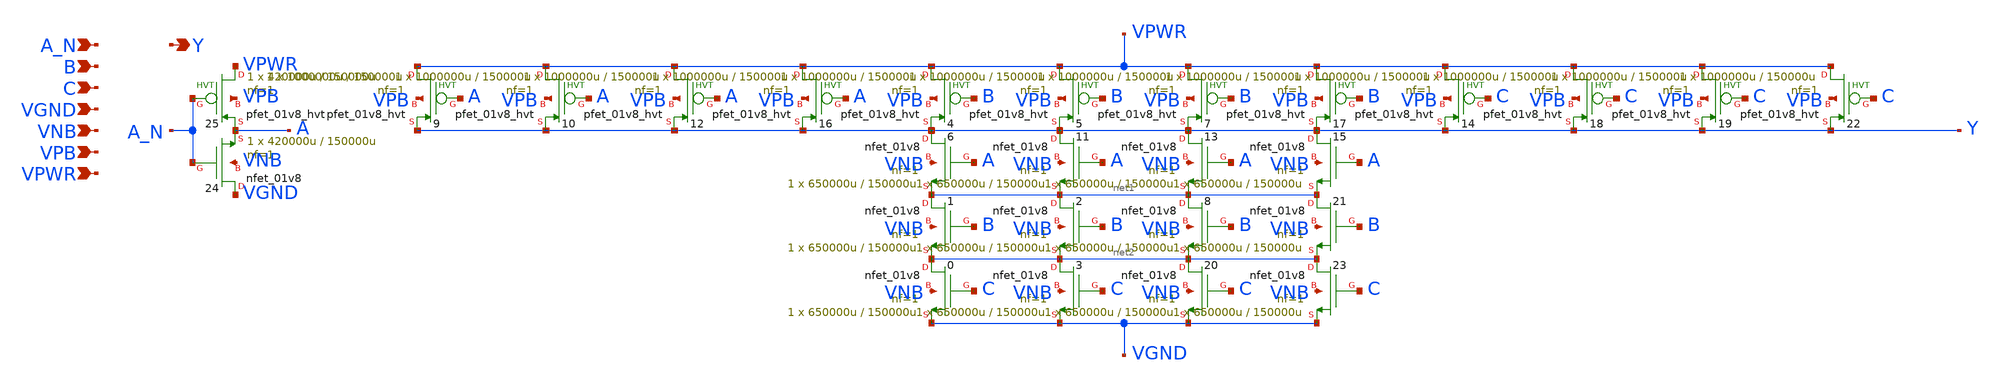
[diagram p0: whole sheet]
** sch_path: schematics/nand3b/sky130_fd_sc_hd__nand3b_4.sch
**.subckt sky130_fd_sc_hd__nand3b_4 A_N B C VGND VNB VPB VPWR Y
*.ipin A_N
*.ipin B
*.ipin C
*.ipin VGND
*.ipin VNB
*.ipin VPB
*.ipin VPWR
*.opin Y
X10 VPWR A Y VPB sky130_fd_pr__pfet_01v8_hvt L=150000u W=1000000u nf=1 ad='int((1 + 1)/2) * 1000000u / 1 * 0.29'
+ as='int((1 + 2)/2) * 1000000u / 1 * 0.29' pd='2*int((1 + 1)/2) * (1000000u / 1 + 0.29)' ps='2*int((1 + 2)/2) * (1000000u / 1 + 0.29)'
+ nrd='0.29 / 1000000u ' nrs='0.29 / 1000000u ' sa=0 sb=0 sd=0 mult=1 m=1
X9 VPWR A Y VPB sky130_fd_pr__pfet_01v8_hvt L=150000u W=1000000u nf=1 ad='int((1 + 1)/2) * 1000000u / 1 * 0.29'
+ as='int((1 + 2)/2) * 1000000u / 1 * 0.29' pd='2*int((1 + 1)/2) * (1000000u / 1 + 0.29)' ps='2*int((1 + 2)/2) * (1000000u / 1 + 0.29)'
+ nrd='0.29 / 1000000u ' nrs='0.29 / 1000000u ' sa=0 sb=0 sd=0 mult=1 m=1
X6 Y A net1 VNB sky130_fd_pr__nfet_01v8 L=150000u W=650000u nf=1 ad='int((1 + 1)/2) * 650000u / 1 * 0.29'
+ as='int((1 + 2)/2) * 650000u / 1 * 0.29' pd='2*int((1 + 1)/2) * (650000u / 1 + 0.29)' ps='2*int((1 + 2)/2) * (650000u / 1 + 0.29)'
+ nrd='0.29 / 650000u ' nrs='0.29 / 650000u ' sa=0 sb=0 sd=0 mult=1 m=1
X1 net1 B net2 VNB sky130_fd_pr__nfet_01v8 L=150000u W=650000u nf=1 ad='int((1 + 1)/2) * 650000u / 1 * 0.29'
+ as='int((1 + 2)/2) * 650000u / 1 * 0.29' pd='2*int((1 + 1)/2) * (650000u / 1 + 0.29)' ps='2*int((1 + 2)/2) * (650000u / 1 + 0.29)'
+ nrd='0.29 / 650000u ' nrs='0.29 / 650000u ' sa=0 sb=0 sd=0 mult=1 m=1
X12 VPWR A Y VPB sky130_fd_pr__pfet_01v8_hvt L=150000u W=1000000u nf=1 ad='int((1 + 1)/2) * 1000000u / 1 * 0.29'
+ as='int((1 + 2)/2) * 1000000u / 1 * 0.29' pd='2*int((1 + 1)/2) * (1000000u / 1 + 0.29)' ps='2*int((1 + 2)/2) * (1000000u / 1 + 0.29)'
+ nrd='0.29 / 1000000u ' nrs='0.29 / 1000000u ' sa=0 sb=0 sd=0 mult=1 m=1
X0 net2 C VGND VNB sky130_fd_pr__nfet_01v8 L=150000u W=650000u nf=1 ad='int((1 + 1)/2) * 650000u / 1 * 0.29'
+ as='int((1 + 2)/2) * 650000u / 1 * 0.29' pd='2*int((1 + 1)/2) * (650000u / 1 + 0.29)' ps='2*int((1 + 2)/2) * (650000u / 1 + 0.29)'
+ nrd='0.29 / 650000u ' nrs='0.29 / 650000u ' sa=0 sb=0 sd=0 mult=1 m=1
X4 VPWR B Y VPB sky130_fd_pr__pfet_01v8_hvt L=150000u W=1000000u nf=1 ad='int((1 + 1)/2) * 1000000u / 1 * 0.29'
+ as='int((1 + 2)/2) * 1000000u / 1 * 0.29' pd='2*int((1 + 1)/2) * (1000000u / 1 + 0.29)' ps='2*int((1 + 2)/2) * (1000000u / 1 + 0.29)'
+ nrd='0.29 / 1000000u ' nrs='0.29 / 1000000u ' sa=0 sb=0 sd=0 mult=1 m=1
X16 VPWR A Y VPB sky130_fd_pr__pfet_01v8_hvt L=150000u W=1000000u nf=1 ad='int((1 + 1)/2) * 1000000u / 1 * 0.29'
+ as='int((1 + 2)/2) * 1000000u / 1 * 0.29' pd='2*int((1 + 1)/2) * (1000000u / 1 + 0.29)' ps='2*int((1 + 2)/2) * (1000000u / 1 + 0.29)'
+ nrd='0.29 / 1000000u ' nrs='0.29 / 1000000u ' sa=0 sb=0 sd=0 mult=1 m=1
X5 VPWR B Y VPB sky130_fd_pr__pfet_01v8_hvt L=150000u W=1000000u nf=1 ad='int((1 + 1)/2) * 1000000u / 1 * 0.29'
+ as='int((1 + 2)/2) * 1000000u / 1 * 0.29' pd='2*int((1 + 1)/2) * (1000000u / 1 + 0.29)' ps='2*int((1 + 2)/2) * (1000000u / 1 + 0.29)'
+ nrd='0.29 / 1000000u ' nrs='0.29 / 1000000u ' sa=0 sb=0 sd=0 mult=1 m=1
X11 Y A net1 VNB sky130_fd_pr__nfet_01v8 L=150000u W=650000u nf=1 ad='int((1 + 1)/2) * 650000u / 1 * 0.29'
+ as='int((1 + 2)/2) * 650000u / 1 * 0.29' pd='2*int((1 + 1)/2) * (650000u / 1 + 0.29)' ps='2*int((1 + 2)/2) * (650000u / 1 + 0.29)'
+ nrd='0.29 / 650000u ' nrs='0.29 / 650000u ' sa=0 sb=0 sd=0 mult=1 m=1
X2 net1 B net2 VNB sky130_fd_pr__nfet_01v8 L=150000u W=650000u nf=1 ad='int((1 + 1)/2) * 650000u / 1 * 0.29'
+ as='int((1 + 2)/2) * 650000u / 1 * 0.29' pd='2*int((1 + 1)/2) * (650000u / 1 + 0.29)' ps='2*int((1 + 2)/2) * (650000u / 1 + 0.29)'
+ nrd='0.29 / 650000u ' nrs='0.29 / 650000u ' sa=0 sb=0 sd=0 mult=1 m=1
X3 net2 C VGND VNB sky130_fd_pr__nfet_01v8 L=150000u W=650000u nf=1 ad='int((1 + 1)/2) * 650000u / 1 * 0.29'
+ as='int((1 + 2)/2) * 650000u / 1 * 0.29' pd='2*int((1 + 1)/2) * (650000u / 1 + 0.29)' ps='2*int((1 + 2)/2) * (650000u / 1 + 0.29)'
+ nrd='0.29 / 650000u ' nrs='0.29 / 650000u ' sa=0 sb=0 sd=0 mult=1 m=1
X17 VPWR B Y VPB sky130_fd_pr__pfet_01v8_hvt L=150000u W=1000000u nf=1 ad='int((1 + 1)/2) * 1000000u / 1 * 0.29'
+ as='int((1 + 2)/2) * 1000000u / 1 * 0.29' pd='2*int((1 + 1)/2) * (1000000u / 1 + 0.29)' ps='2*int((1 + 2)/2) * (1000000u / 1 + 0.29)'
+ nrd='0.29 / 1000000u ' nrs='0.29 / 1000000u ' sa=0 sb=0 sd=0 mult=1 m=1
X7 VPWR B Y VPB sky130_fd_pr__pfet_01v8_hvt L=150000u W=1000000u nf=1 ad='int((1 + 1)/2) * 1000000u / 1 * 0.29'
+ as='int((1 + 2)/2) * 1000000u / 1 * 0.29' pd='2*int((1 + 1)/2) * (1000000u / 1 + 0.29)' ps='2*int((1 + 2)/2) * (1000000u / 1 + 0.29)'
+ nrd='0.29 / 1000000u ' nrs='0.29 / 1000000u ' sa=0 sb=0 sd=0 mult=1 m=1
X14 VPWR C Y VPB sky130_fd_pr__pfet_01v8_hvt L=150000u W=1000000u nf=1 ad='int((1 + 1)/2) * 1000000u / 1 * 0.29'
+ as='int((1 + 2)/2) * 1000000u / 1 * 0.29' pd='2*int((1 + 1)/2) * (1000000u / 1 + 0.29)' ps='2*int((1 + 2)/2) * (1000000u / 1 + 0.29)'
+ nrd='0.29 / 1000000u ' nrs='0.29 / 1000000u ' sa=0 sb=0 sd=0 mult=1 m=1
X19 VPWR C Y VPB sky130_fd_pr__pfet_01v8_hvt L=150000u W=1000000u nf=1 ad='int((1 + 1)/2) * 1000000u / 1 * 0.29'
+ as='int((1 + 2)/2) * 1000000u / 1 * 0.29' pd='2*int((1 + 1)/2) * (1000000u / 1 + 0.29)' ps='2*int((1 + 2)/2) * (1000000u / 1 + 0.29)'
+ nrd='0.29 / 1000000u ' nrs='0.29 / 1000000u ' sa=0 sb=0 sd=0 mult=1 m=1
X18 VPWR C Y VPB sky130_fd_pr__pfet_01v8_hvt L=150000u W=1000000u nf=1 ad='int((1 + 1)/2) * 1000000u / 1 * 0.29'
+ as='int((1 + 2)/2) * 1000000u / 1 * 0.29' pd='2*int((1 + 1)/2) * (1000000u / 1 + 0.29)' ps='2*int((1 + 2)/2) * (1000000u / 1 + 0.29)'
+ nrd='0.29 / 1000000u ' nrs='0.29 / 1000000u ' sa=0 sb=0 sd=0 mult=1 m=1
X22 VPWR C Y VPB sky130_fd_pr__pfet_01v8_hvt L=150000u W=1000000u nf=1 ad='int((1 + 1)/2) * 1000000u / 1 * 0.29'
+ as='int((1 + 2)/2) * 1000000u / 1 * 0.29' pd='2*int((1 + 1)/2) * (1000000u / 1 + 0.29)' ps='2*int((1 + 2)/2) * (1000000u / 1 + 0.29)'
+ nrd='0.29 / 1000000u ' nrs='0.29 / 1000000u ' sa=0 sb=0 sd=0 mult=1 m=1
X13 Y A net1 VNB sky130_fd_pr__nfet_01v8 L=150000u W=650000u nf=1 ad='int((1 + 1)/2) * 650000u / 1 * 0.29'
+ as='int((1 + 2)/2) * 650000u / 1 * 0.29' pd='2*int((1 + 1)/2) * (650000u / 1 + 0.29)' ps='2*int((1 + 2)/2) * (650000u / 1 + 0.29)'
+ nrd='0.29 / 650000u ' nrs='0.29 / 650000u ' sa=0 sb=0 sd=0 mult=1 m=1
X8 net1 B net2 VNB sky130_fd_pr__nfet_01v8 L=150000u W=650000u nf=1 ad='int((1 + 1)/2) * 650000u / 1 * 0.29'
+ as='int((1 + 2)/2) * 650000u / 1 * 0.29' pd='2*int((1 + 1)/2) * (650000u / 1 + 0.29)' ps='2*int((1 + 2)/2) * (650000u / 1 + 0.29)'
+ nrd='0.29 / 650000u ' nrs='0.29 / 650000u ' sa=0 sb=0 sd=0 mult=1 m=1
X20 net2 C VGND VNB sky130_fd_pr__nfet_01v8 L=150000u W=650000u nf=1 ad='int((1 + 1)/2) * 650000u / 1 * 0.29'
+ as='int((1 + 2)/2) * 650000u / 1 * 0.29' pd='2*int((1 + 1)/2) * (650000u / 1 + 0.29)' ps='2*int((1 + 2)/2) * (650000u / 1 + 0.29)'
+ nrd='0.29 / 650000u ' nrs='0.29 / 650000u ' sa=0 sb=0 sd=0 mult=1 m=1
X15 Y A net1 VNB sky130_fd_pr__nfet_01v8 L=150000u W=650000u nf=1 ad='int((1 + 1)/2) * 650000u / 1 * 0.29'
+ as='int((1 + 2)/2) * 650000u / 1 * 0.29' pd='2*int((1 + 1)/2) * (650000u / 1 + 0.29)' ps='2*int((1 + 2)/2) * (650000u / 1 + 0.29)'
+ nrd='0.29 / 650000u ' nrs='0.29 / 650000u ' sa=0 sb=0 sd=0 mult=1 m=1
X21 net1 B net2 VNB sky130_fd_pr__nfet_01v8 L=150000u W=650000u nf=1 ad='int((1 + 1)/2) * 650000u / 1 * 0.29'
+ as='int((1 + 2)/2) * 650000u / 1 * 0.29' pd='2*int((1 + 1)/2) * (650000u / 1 + 0.29)' ps='2*int((1 + 2)/2) * (650000u / 1 + 0.29)'
+ nrd='0.29 / 650000u ' nrs='0.29 / 650000u ' sa=0 sb=0 sd=0 mult=1 m=1
X23 net2 C VGND VNB sky130_fd_pr__nfet_01v8 L=150000u W=650000u nf=1 ad='int((1 + 1)/2) * 650000u / 1 * 0.29'
+ as='int((1 + 2)/2) * 650000u / 1 * 0.29' pd='2*int((1 + 1)/2) * (650000u / 1 + 0.29)' ps='2*int((1 + 2)/2) * (650000u / 1 + 0.29)'
+ nrd='0.29 / 650000u ' nrs='0.29 / 650000u ' sa=0 sb=0 sd=0 mult=1 m=1
X24 VGND A_N A VNB sky130_fd_pr__nfet_01v8 L=150000u W=420000u nf=1 ad='int((1 + 1)/2) * 420000u / 1 * 0.29'
+ as='int((1 + 2)/2) * 420000u / 1 * 0.29' pd='2*int((1 + 1)/2) * (420000u / 1 + 0.29)' ps='2*int((1 + 2)/2) * (420000u / 1 + 0.29)'
+ nrd='0.29 / 420000u ' nrs='0.29 / 420000u ' sa=0 sb=0 sd=0 mult=1 m=1
X25 VPWR A_N A VPB sky130_fd_pr__pfet_01v8_hvt L=150000u W=420000u nf=1 ad='int((1 + 1)/2) * 420000u / 1 * 0.29'
+ as='int((1 + 2)/2) * 420000u / 1 * 0.29' pd='2*int((1 + 1)/2) * (420000u / 1 + 0.29)' ps='2*int((1 + 2)/2) * (420000u / 1 + 0.29)'
+ nrd='0.29 / 420000u ' nrs='0.29 / 420000u ' sa=0 sb=0 sd=0 mult=1 m=1
**.ends
.end
